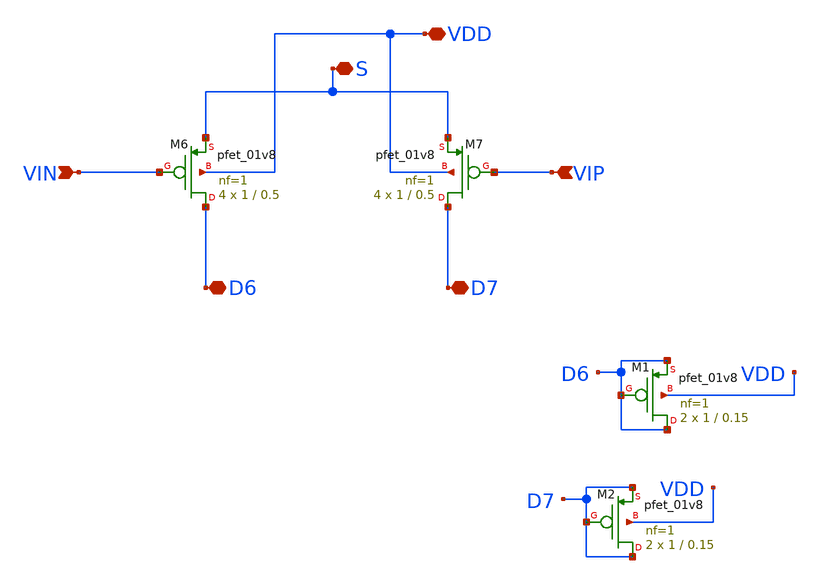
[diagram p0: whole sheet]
** sch_path: opamp/mag/pmos67.sch
**.subckt pmos67 VIP VIN VDD D6 D7 S
*.ipin VIP
*.ipin VIN
*.iopin VDD
*.iopin D6
*.iopin D7
*.iopin S
XM6 D6 VIN S VDD sky130_fd_pr__pfet_01v8 L=0.5 W=1 nf=1 ad='int((nf+1)/2) * W/nf * 0.29' as='int((nf+2)/2) * W/nf * 0.29'
+ pd='2*int((nf+1)/2) * (W/nf + 0.29)' ps='2*int((nf+2)/2) * (W/nf + 0.29)' nrd='0.29 / W' nrs='0.29 / W'
+ sa=0 sb=0 sd=0 mult=4 m=4
XM7 D7 VIP S VDD sky130_fd_pr__pfet_01v8 L=0.5 W=1 nf=1 ad='int((nf+1)/2) * W/nf * 0.29' as='int((nf+2)/2) * W/nf * 0.29'
+ pd='2*int((nf+1)/2) * (W/nf + 0.29)' ps='2*int((nf+2)/2) * (W/nf + 0.29)' nrd='0.29 / W' nrs='0.29 / W'
+ sa=0 sb=0 sd=0 mult=4 m=4
XM1 D6 D6 D6 VDD sky130_fd_pr__pfet_01v8 L=0.15 W=1 nf=1 ad='int((nf+1)/2) * W/nf * 0.29' as='int((nf+2)/2) * W/nf * 0.29'
+ pd='2*int((nf+1)/2) * (W/nf + 0.29)' ps='2*int((nf+2)/2) * (W/nf + 0.29)' nrd='0.29 / W' nrs='0.29 / W'
+ sa=0 sb=0 sd=0 mult=2 m=2
XM2 D7 D7 D7 VDD sky130_fd_pr__pfet_01v8 L=0.15 W=1 nf=1 ad='int((nf+1)/2) * W/nf * 0.29' as='int((nf+2)/2) * W/nf * 0.29'
+ pd='2*int((nf+1)/2) * (W/nf + 0.29)' ps='2*int((nf+2)/2) * (W/nf + 0.29)' nrd='0.29 / W' nrs='0.29 / W'
+ sa=0 sb=0 sd=0 mult=2 m=2
**.ends
.end
